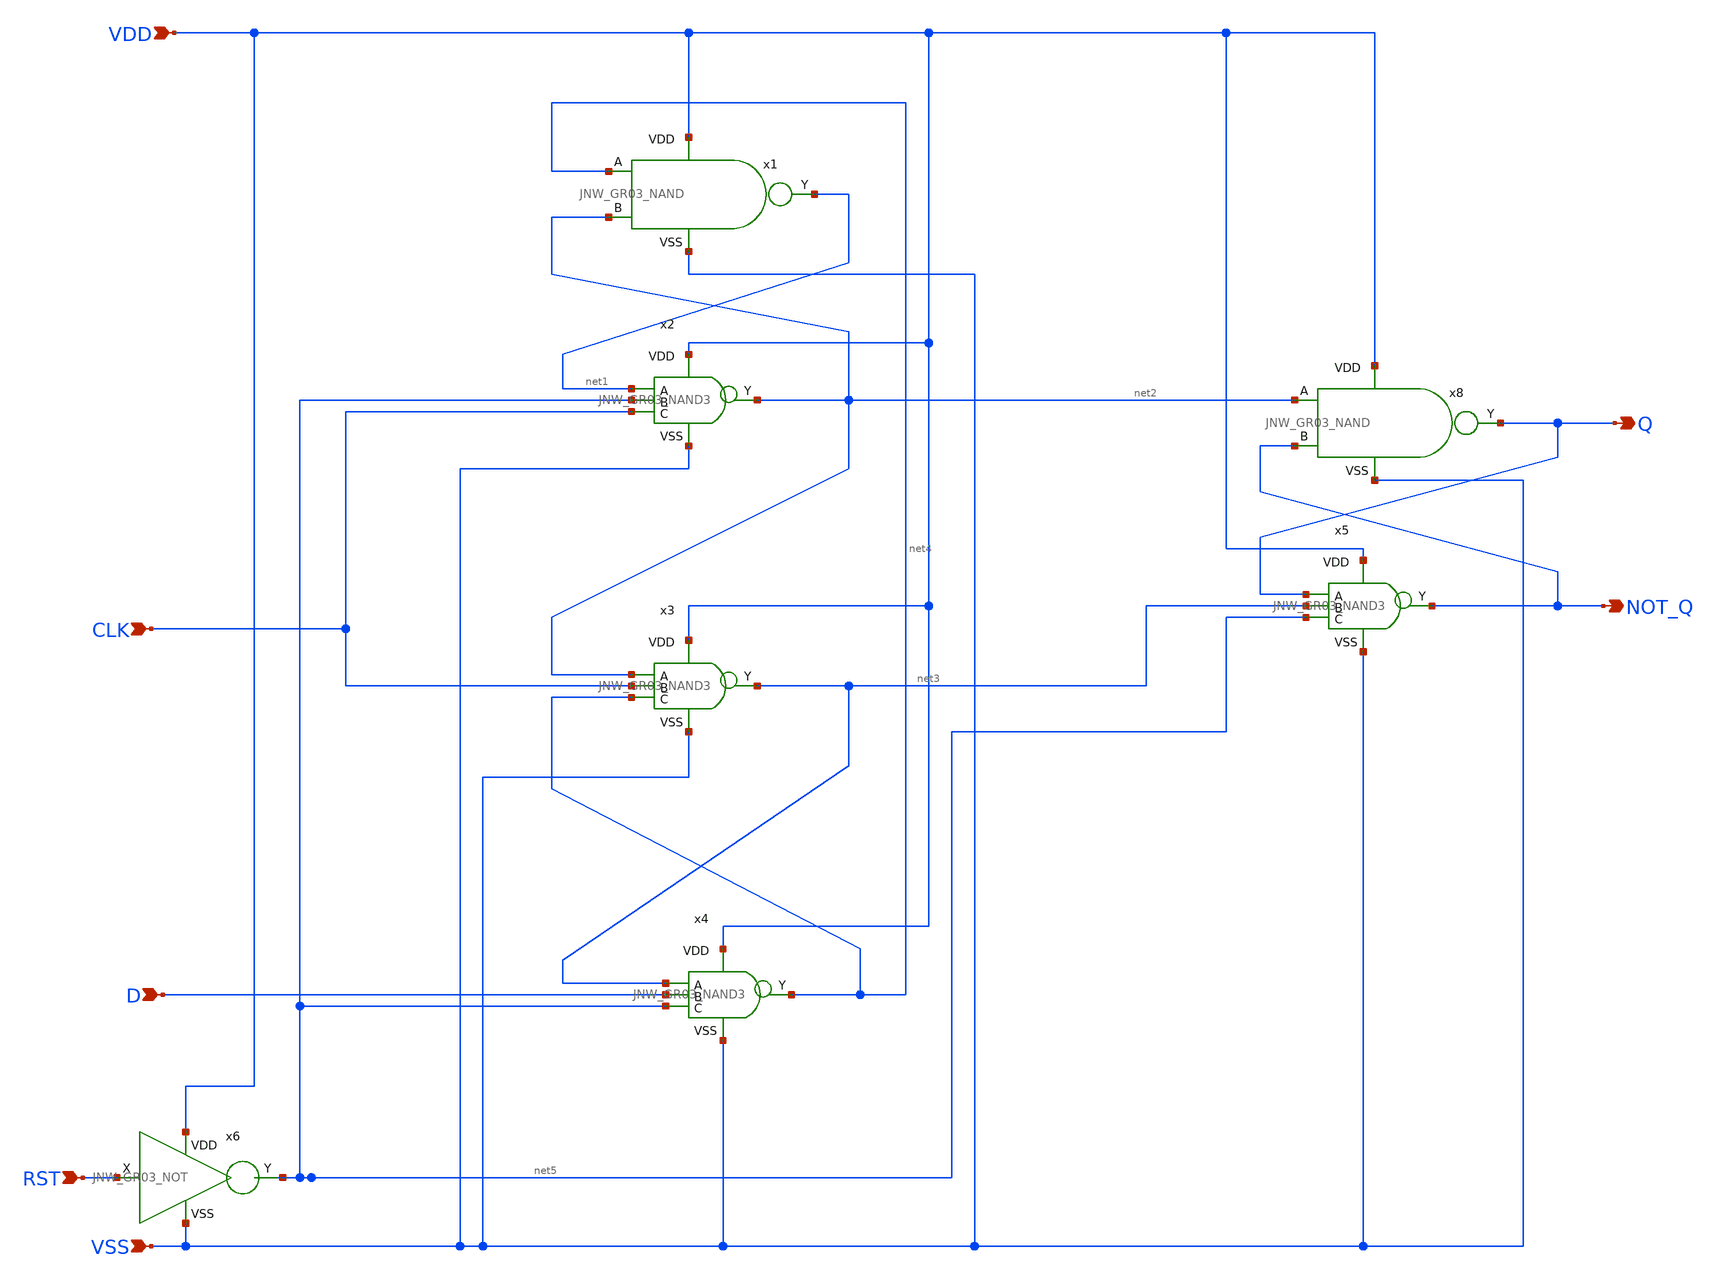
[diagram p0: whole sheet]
** sch_path: design/JNW_GR03_SKY130A/JNW_GR03_DFLIPFLOP_R_R.sch
**.subckt JNW_GR03_DFLIPFLOP_R_R Q RST CLK VSS D NOT_Q VDD
*.opin Q
*.ipin RST
*.ipin CLK
*.ipin VSS
*.ipin D
*.opin NOT_Q
*.ipin VDD
x1 VDD net1 net4 net2 VSS JNW_GR03_NAND
x8 VDD Q net2 NOT_Q VSS JNW_GR03_NAND
x2 VDD net1 net5 net2 CLK VSS JNW_GR03_NAND3
x3 VDD net2 CLK net3 net4 VSS JNW_GR03_NAND3
x4 VDD net3 D net4 net5 VSS JNW_GR03_NAND3
x5 VDD Q net3 NOT_Q net5 VSS JNW_GR03_NAND3
x6 VDD RST net5 VSS JNW_GR03_NOT
**.ends
.end
